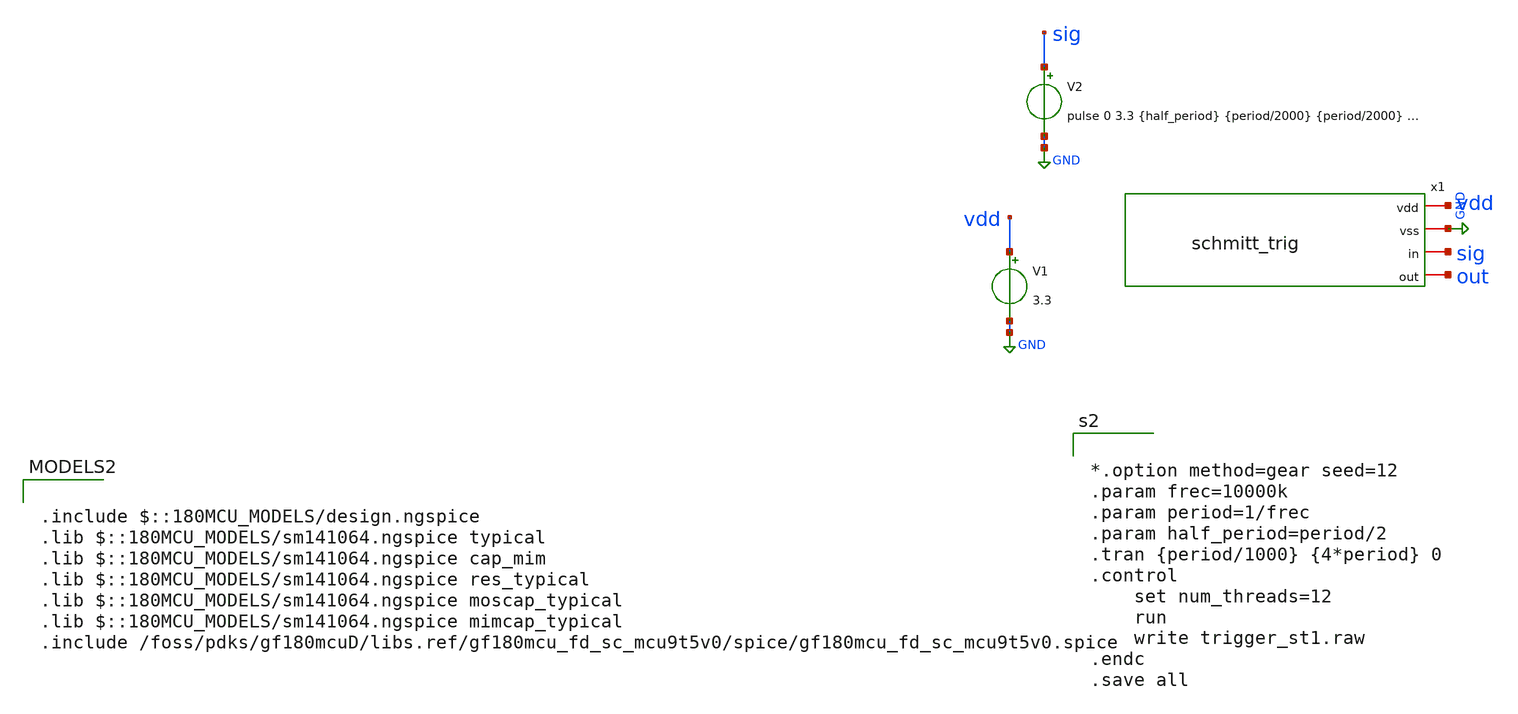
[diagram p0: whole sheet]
** sch_path: designs/libs/tb_schmitt_trig/schmitt_trig.sch
**.subckt schmitt_trig
V2 sig GND pulse 0 3.3 {half_period} {period/2000} {period/2000} {half_period} {period}
V1 vdd GND 3.3
x1 vdd GND sig out schmitt_trig
**** begin user architecture code

.include $::180MCU_MODELS/design.ngspice
.lib $::180MCU_MODELS/sm141064.ngspice typical
.lib $::180MCU_MODELS/sm141064.ngspice cap_mim
.lib $::180MCU_MODELS/sm141064.ngspice res_typical
.lib $::180MCU_MODELS/sm141064.ngspice moscap_typical
.lib $::180MCU_MODELS/sm141064.ngspice mimcap_typical
.include /foss/pdks/gf180mcuD/libs.ref/gf180mcu_fd_sc_mcu9t5v0/spice/gf180mcu_fd_sc_mcu9t5v0.spice



*.option method=gear seed=12
.param frec=10000k
.param period=1/frec
.param half_period=period/2
.tran {period/1000} {4*period} 0
.control
	set num_threads=12
	run
	write trigger_st1.raw
.endc
.save all


**** end user architecture code
**.ends
.GLOBAL GND
.end
